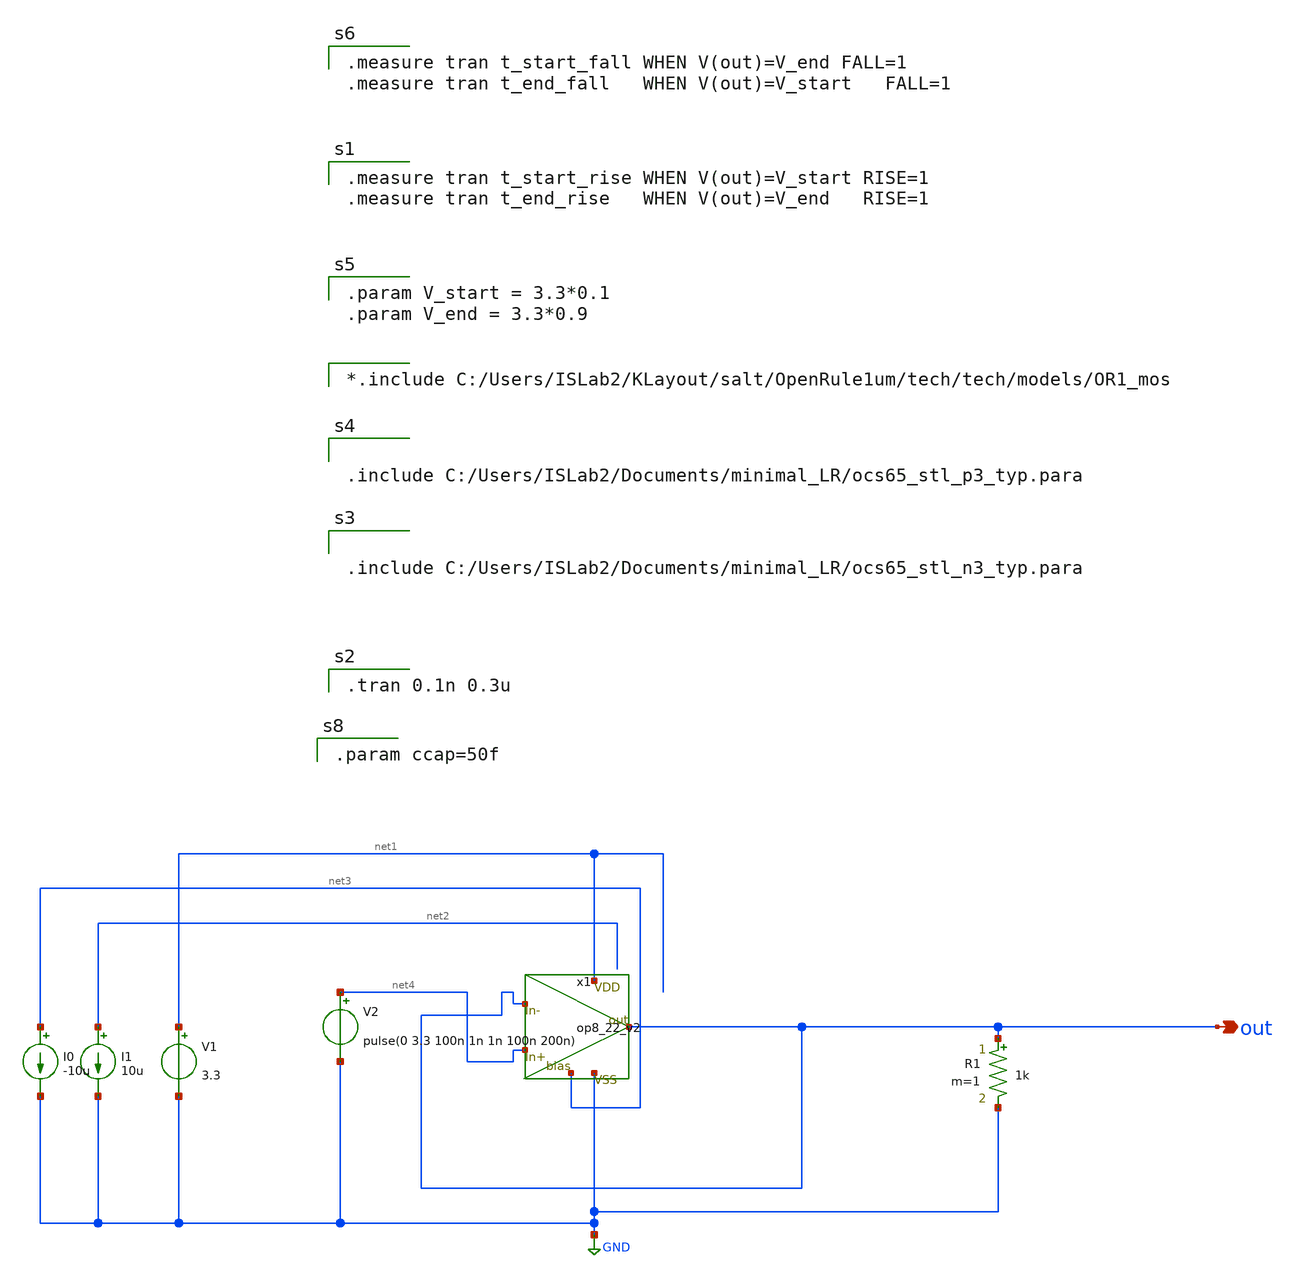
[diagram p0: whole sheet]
** sch_path: OPAmp_sim_SR.sch
**.subckt OPAmp_sim_SR out
*.opin out
V1 net1 GND 3.3
I0 net3 GND -10u
V2 net4 GND pulse(0 3.3 100n 1n 1n 100n 200n)
I1 net2 GND 10u
x1 net4 out net1 GND net3 out op8_22_v2
R1 out GND 1k m=1
**** begin user architecture code


.include C:/Users/ISLab2/Documents/minimal_LR/ocs65_stl_n3_typ.para



.include C:/Users/ISLab2/Documents/minimal_LR/ocs65_stl_p3_typ.para


.tran 0.1n 0.3u


.param V_start = 3.3*0.1
.param V_end = 3.3*0.9


.measure tran t_start_rise WHEN V(out)=V_start RISE=1
.measure tran t_end_rise   WHEN V(out)=V_end   RISE=1


.measure tran t_start_fall WHEN V(out)=V_end FALL=1
.measure tran t_end_fall   WHEN V(out)=V_start   FALL=1


.param ccap=50f


*.include C:/Users/ISLab2/KLayout/salt/OpenRule1um/tech/tech/models/OR1_mos

**** end user architecture code
**.ends
.GLOBAL GND
.end
